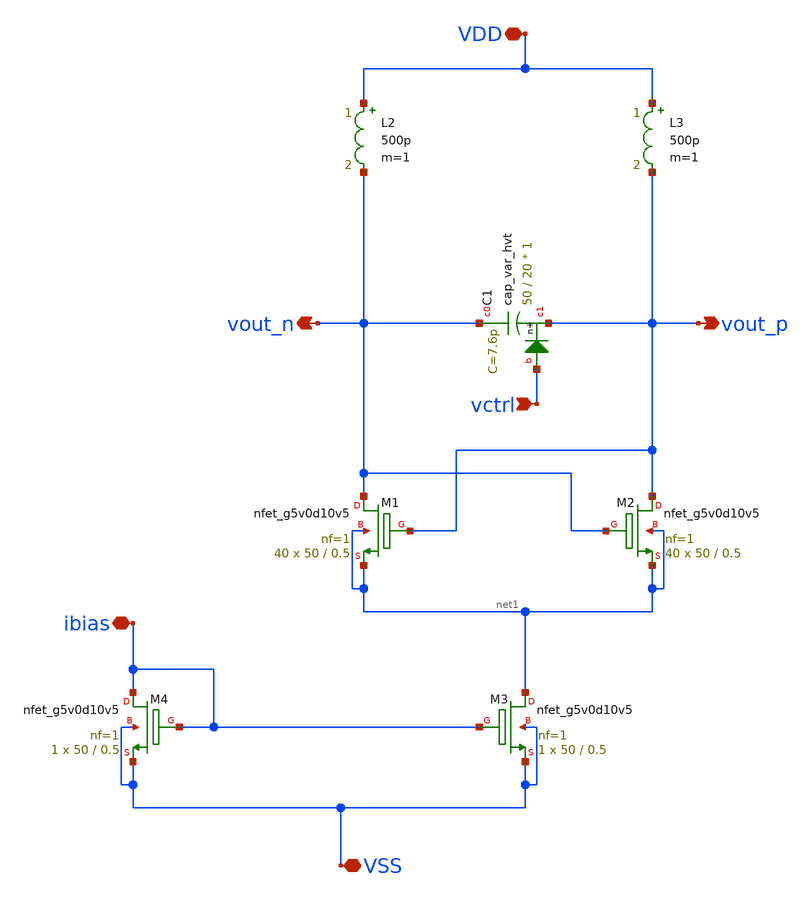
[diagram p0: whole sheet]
** sch_path: designs/libs/test_vco/lc_osc.sch
* Copyright 2021 Stefan Frederik Schippers
* Licensed under the Apache License, Version 2.0 (the "License");
* you may not use this file except in compliance with the License.
* You may obtain a copy of the License at
* https://www.apache.org/licenses/LICENSE-2.0
* Unless required by applicable law or agreed to in writing, software
* distributed under the License is distributed on an "AS IS" BASIS,
* WITHOUT WARRANTIES OR CONDITIONS OF ANY KIND, either express or implied.
* See the License for the specific language governing permissions and
* limitations under the License.
**.subckt lc_osc vctrl VSS VDD vout_p vout_n ibias
*.ipin vctrl
*.iopin VSS
*.iopin VDD
*.opin vout_p
*.opin vout_n
*.iopin ibias
L2 VDD vout_n 500p m=1
L3 VDD vout_p 500p m=1
XM4 ibias ibias VSS VSS sky130_fd_pr__nfet_g5v0d10v5 L=0.5 W=50 nf=1 ad='int((nf+1)/2) * W/nf * 0.29'
+ as='int((nf+2)/2) * W/nf * 0.29' pd='2*int((nf+1)/2) * (W/nf + 0.29)' ps='2*int((nf+2)/2) * (W/nf + 0.29)'
+ nrd='0.29 / W' nrs='0.29 / W' sa=0 sb=0 sd=0 mult=1 m=1
XM3 net1 ibias VSS VSS sky130_fd_pr__nfet_g5v0d10v5 L=0.5 W=50 nf=1 ad='int((nf+1)/2) * W/nf * 0.29'
+ as='int((nf+2)/2) * W/nf * 0.29' pd='2*int((nf+1)/2) * (W/nf + 0.29)' ps='2*int((nf+2)/2) * (W/nf + 0.29)'
+ nrd='0.29 / W' nrs='0.29 / W' sa=0 sb=0 sd=0 mult=1 m=1
XM1 vout_n vout_p net1 net1 sky130_fd_pr__nfet_g5v0d10v5 L=0.5 W=50 nf=1 ad='int((nf+1)/2) * W/nf * 0.29'
+ as='int((nf+2)/2) * W/nf * 0.29' pd='2*int((nf+1)/2) * (W/nf + 0.29)' ps='2*int((nf+2)/2) * (W/nf + 0.29)'
+ nrd='0.29 / W' nrs='0.29 / W' sa=0 sb=0 sd=0 mult=40 m=40
XM2 vout_p vout_n net1 net1 sky130_fd_pr__nfet_g5v0d10v5 L=0.5 W=50 nf=1 ad='int((nf+1)/2) * W/nf * 0.29'
+ as='int((nf+2)/2) * W/nf * 0.29' pd='2*int((nf+1)/2) * (W/nf + 0.29)' ps='2*int((nf+2)/2) * (W/nf + 0.29)'
+ nrd='0.29 / W' nrs='0.29 / W' sa=0 sb=0 sd=0 mult=40 m=40
XC1 vout_n vout_p vctrl sky130_fd_pr__cap_var_hvt W=50 L=20 VM=1 m=1
**.ends
.end
